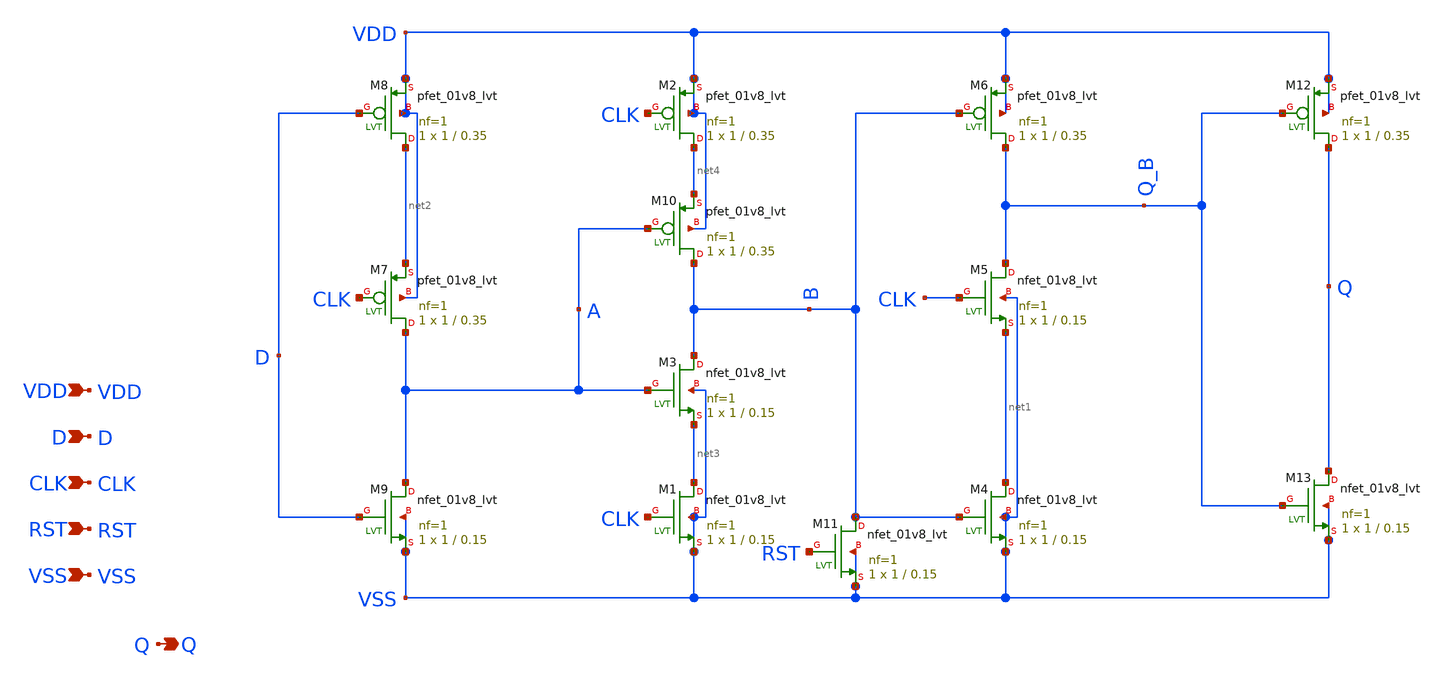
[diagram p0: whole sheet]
** sch_path: design/LELO_SVOD_SKY130A/LELO_TSPC.sch
**.subckt LELO_TSPC D CLK VDD VSS Q RST
*.ipin D
*.ipin CLK
*.ipin VDD
*.ipin VSS
*.opin Q
*.ipin RST
XM1 net3 CLK VSS VSS sky130_fd_pr__nfet_01v8_lvt L=0.15 W=1 nf=1 ad='int((1 + 1)/2) * 1 / 1 * 0.29' as='int((1 + 2)/2) * 1 / 1 * 0.29'
+ pd='2*int((1 + 1)/2) * (1 / 1 + 0.29)' ps='2*int((1 + 2)/2) * (1 / 1 + 0.29)' nrd='0.29 / 1 ' nrs='0.29 / 1 '
+ sa=0 sb=0 sd=0 mult=1 m=1
XM5 Q_B CLK net1 VSS sky130_fd_pr__nfet_01v8_lvt L=0.15 W=1 nf=1 ad='int((1 + 1)/2) * 1 / 1 * 0.29' as='int((1 + 2)/2) * 1 / 1 * 0.29'
+ pd='2*int((1 + 1)/2) * (1 / 1 + 0.29)' ps='2*int((1 + 2)/2) * (1 / 1 + 0.29)' nrd='0.29 / 1 ' nrs='0.29 / 1 '
+ sa=0 sb=0 sd=0 mult=1 m=1
XM6 Q_B B VDD VDD sky130_fd_pr__pfet_01v8_lvt L=0.35 W=1 nf=1 ad='int((1 + 1)/2) * 1 / 1 * 0.29' as='int((1 + 2)/2) * 1 / 1 * 0.29'
+ pd='2*int((1 + 1)/2) * (1 / 1 + 0.29)' ps='2*int((1 + 2)/2) * (1 / 1 + 0.29)' nrd='0.29 / 1 ' nrs='0.29 / 1 '
+ sa=0 sb=0 sd=0 mult=1 m=1
XM2 net4 CLK VDD VDD sky130_fd_pr__pfet_01v8_lvt L=0.35 W=1 nf=1 ad='int((1 + 1)/2) * 1 / 1 * 0.29' as='int((1 + 2)/2) * 1 / 1 * 0.29'
+ pd='2*int((1 + 1)/2) * (1 / 1 + 0.29)' ps='2*int((1 + 2)/2) * (1 / 1 + 0.29)' nrd='0.29 / 1 ' nrs='0.29 / 1 '
+ sa=0 sb=0 sd=0 mult=1 m=1
XM4 net1 B VSS VSS sky130_fd_pr__nfet_01v8_lvt L=0.15 W=1 nf=1 ad='int((1 + 1)/2) * 1 / 1 * 0.29' as='int((1 + 2)/2) * 1 / 1 * 0.29'
+ pd='2*int((1 + 1)/2) * (1 / 1 + 0.29)' ps='2*int((1 + 2)/2) * (1 / 1 + 0.29)' nrd='0.29 / 1 ' nrs='0.29 / 1 '
+ sa=0 sb=0 sd=0 mult=1 m=1
XM3 B A net3 VSS sky130_fd_pr__nfet_01v8_lvt L=0.15 W=1 nf=1 ad='int((1 + 1)/2) * 1 / 1 * 0.29' as='int((1 + 2)/2) * 1 / 1 * 0.29'
+ pd='2*int((1 + 1)/2) * (1 / 1 + 0.29)' ps='2*int((1 + 2)/2) * (1 / 1 + 0.29)' nrd='0.29 / 1 ' nrs='0.29 / 1 '
+ sa=0 sb=0 sd=0 mult=1 m=1
XM7 A CLK net2 VDD sky130_fd_pr__pfet_01v8_lvt L=0.35 W=1 nf=1 ad='int((1 + 1)/2) * 1 / 1 * 0.29' as='int((1 + 2)/2) * 1 / 1 * 0.29'
+ pd='2*int((1 + 1)/2) * (1 / 1 + 0.29)' ps='2*int((1 + 2)/2) * (1 / 1 + 0.29)' nrd='0.29 / 1 ' nrs='0.29 / 1 '
+ sa=0 sb=0 sd=0 mult=1 m=1
XM8 net2 D VDD VDD sky130_fd_pr__pfet_01v8_lvt L=0.35 W=1 nf=1 ad='int((1 + 1)/2) * 1 / 1 * 0.29' as='int((1 + 2)/2) * 1 / 1 * 0.29'
+ pd='2*int((1 + 1)/2) * (1 / 1 + 0.29)' ps='2*int((1 + 2)/2) * (1 / 1 + 0.29)' nrd='0.29 / 1 ' nrs='0.29 / 1 '
+ sa=0 sb=0 sd=0 mult=1 m=1
XM9 A D VSS VSS sky130_fd_pr__nfet_01v8_lvt L=0.15 W=1 nf=1 ad='int((1 + 1)/2) * 1 / 1 * 0.29' as='int((1 + 2)/2) * 1 / 1 * 0.29'
+ pd='2*int((1 + 1)/2) * (1 / 1 + 0.29)' ps='2*int((1 + 2)/2) * (1 / 1 + 0.29)' nrd='0.29 / 1 ' nrs='0.29 / 1 '
+ sa=0 sb=0 sd=0 mult=1 m=1
XM10 B A net4 VDD sky130_fd_pr__pfet_01v8_lvt L=0.35 W=1 nf=1 ad='int((1 + 1)/2) * 1 / 1 * 0.29' as='int((1 + 2)/2) * 1 / 1 * 0.29'
+ pd='2*int((1 + 1)/2) * (1 / 1 + 0.29)' ps='2*int((1 + 2)/2) * (1 / 1 + 0.29)' nrd='0.29 / 1 ' nrs='0.29 / 1 '
+ sa=0 sb=0 sd=0 mult=1 m=1
XM11 B RST VSS VSS sky130_fd_pr__nfet_01v8_lvt L=0.15 W=1 nf=1 ad='int((1 + 1)/2) * 1 / 1 * 0.29' as='int((1 + 2)/2) * 1 / 1 * 0.29'
+ pd='2*int((1 + 1)/2) * (1 / 1 + 0.29)' ps='2*int((1 + 2)/2) * (1 / 1 + 0.29)' nrd='0.29 / 1 ' nrs='0.29 / 1 '
+ sa=0 sb=0 sd=0 mult=1 m=1
XM12 Q Q_B VDD VDD sky130_fd_pr__pfet_01v8_lvt L=0.35 W=1 nf=1 ad='int((1 + 1)/2) * 1 / 1 * 0.29' as='int((1 + 2)/2) * 1 / 1 * 0.29'
+ pd='2*int((1 + 1)/2) * (1 / 1 + 0.29)' ps='2*int((1 + 2)/2) * (1 / 1 + 0.29)' nrd='0.29 / 1 ' nrs='0.29 / 1 '
+ sa=0 sb=0 sd=0 mult=1 m=1
XM13 Q Q_B VSS VSS sky130_fd_pr__nfet_01v8_lvt L=0.15 W=1 nf=1 ad='int((1 + 1)/2) * 1 / 1 * 0.29' as='int((1 + 2)/2) * 1 / 1 * 0.29'
+ pd='2*int((1 + 1)/2) * (1 / 1 + 0.29)' ps='2*int((1 + 2)/2) * (1 / 1 + 0.29)' nrd='0.29 / 1 ' nrs='0.29 / 1 '
+ sa=0 sb=0 sd=0 mult=1 m=1
**.ends
.end
